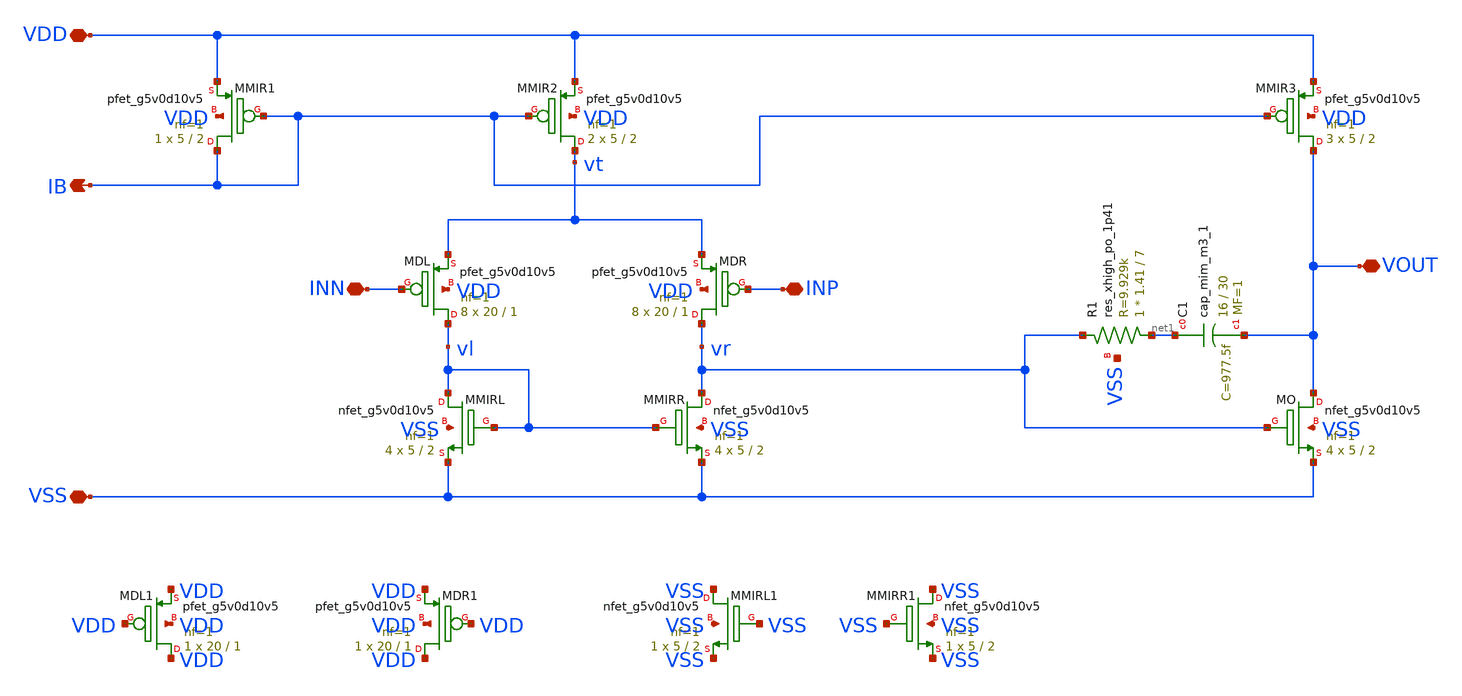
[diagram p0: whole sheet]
** sch_path: tt08/ip/bmbg/xschem/bmbgota.sch
**.subckt bmbgota INP INN VOUT IB VDD VSS
*.iopin INP
*.iopin INN
*.iopin VOUT
*.opin IB
*.iopin VDD
*.iopin VSS
XMDR vr INP vt VDD sky130_fd_pr__pfet_g5v0d10v5 L=1 W=20 nf=1 ad='int((nf+1)/2) * W/nf * 0.29' as='int((nf+2)/2) * W/nf * 0.29'
+ pd='2*int((nf+1)/2) * (W/nf + 0.29)' ps='2*int((nf+2)/2) * (W/nf + 0.29)' nrd='0.29 / W' nrs='0.29 / W'
+ sa=0 sb=0 sd=0 mult=8 m=8
XMMIRL vl vl VSS VSS sky130_fd_pr__nfet_g5v0d10v5 L=2 W=5 nf=1 ad='int((nf+1)/2) * W/nf * 0.29' as='int((nf+2)/2) * W/nf * 0.29'
+ pd='2*int((nf+1)/2) * (W/nf + 0.29)' ps='2*int((nf+2)/2) * (W/nf + 0.29)' nrd='0.29 / W' nrs='0.29 / W'
+ sa=0 sb=0 sd=0 mult=4 m=4
XMMIRR vr vl VSS VSS sky130_fd_pr__nfet_g5v0d10v5 L=2 W=5 nf=1 ad='int((nf+1)/2) * W/nf * 0.29' as='int((nf+2)/2) * W/nf * 0.29'
+ pd='2*int((nf+1)/2) * (W/nf + 0.29)' ps='2*int((nf+2)/2) * (W/nf + 0.29)' nrd='0.29 / W' nrs='0.29 / W'
+ sa=0 sb=0 sd=0 mult=4 m=4
XMDL vl INN vt VDD sky130_fd_pr__pfet_g5v0d10v5 L=1 W=20 nf=1 ad='int((nf+1)/2) * W/nf * 0.29' as='int((nf+2)/2) * W/nf * 0.29'
+ pd='2*int((nf+1)/2) * (W/nf + 0.29)' ps='2*int((nf+2)/2) * (W/nf + 0.29)' nrd='0.29 / W' nrs='0.29 / W'
+ sa=0 sb=0 sd=0 mult=8 m=8
XMMIR2 vt IB VDD VDD sky130_fd_pr__pfet_g5v0d10v5 L=2 W=5 nf=1 ad='int((nf+1)/2) * W/nf * 0.29' as='int((nf+2)/2) * W/nf * 0.29'
+ pd='2*int((nf+1)/2) * (W/nf + 0.29)' ps='2*int((nf+2)/2) * (W/nf + 0.29)' nrd='0.29 / W' nrs='0.29 / W'
+ sa=0 sb=0 sd=0 mult=2 m=2
XMMIR1 IB IB VDD VDD sky130_fd_pr__pfet_g5v0d10v5 L=2 W=5 nf=1 ad='int((nf+1)/2) * W/nf * 0.29' as='int((nf+2)/2) * W/nf * 0.29'
+ pd='2*int((nf+1)/2) * (W/nf + 0.29)' ps='2*int((nf+2)/2) * (W/nf + 0.29)' nrd='0.29 / W' nrs='0.29 / W'
+ sa=0 sb=0 sd=0 mult=1 m=1
XMO VOUT vr VSS VSS sky130_fd_pr__nfet_g5v0d10v5 L=2 W=5 nf=1 ad='int((nf+1)/2) * W/nf * 0.29' as='int((nf+2)/2) * W/nf * 0.29'
+ pd='2*int((nf+1)/2) * (W/nf + 0.29)' ps='2*int((nf+2)/2) * (W/nf + 0.29)' nrd='0.29 / W' nrs='0.29 / W'
+ sa=0 sb=0 sd=0 mult=4 m=4
XMMIR3 VOUT IB VDD VDD sky130_fd_pr__pfet_g5v0d10v5 L=2 W=5 nf=1 ad='int((nf+1)/2) * W/nf * 0.29' as='int((nf+2)/2) * W/nf * 0.29'
+ pd='2*int((nf+1)/2) * (W/nf + 0.29)' ps='2*int((nf+2)/2) * (W/nf + 0.29)' nrd='0.29 / W' nrs='0.29 / W'
+ sa=0 sb=0 sd=0 mult=3 m=3
XR1 net1 vr VSS sky130_fd_pr__res_xhigh_po_1p41 L=7 mult=1 m=1
XC1 net1 VOUT sky130_fd_pr__cap_mim_m3_1 W=16 L=30 MF=1 m=1
XMDL1 VDD VDD VDD VDD sky130_fd_pr__pfet_g5v0d10v5 L=1 W=20 nf=1 ad='int((nf+1)/2) * W/nf * 0.29' as='int((nf+2)/2) * W/nf * 0.29'
+ pd='2*int((nf+1)/2) * (W/nf + 0.29)' ps='2*int((nf+2)/2) * (W/nf + 0.29)' nrd='0.29 / W' nrs='0.29 / W'
+ sa=0 sb=0 sd=0 mult=1 m=1
XMDR1 VDD VDD VDD VDD sky130_fd_pr__pfet_g5v0d10v5 L=1 W=20 nf=1 ad='int((nf+1)/2) * W/nf * 0.29' as='int((nf+2)/2) * W/nf * 0.29'
+ pd='2*int((nf+1)/2) * (W/nf + 0.29)' ps='2*int((nf+2)/2) * (W/nf + 0.29)' nrd='0.29 / W' nrs='0.29 / W'
+ sa=0 sb=0 sd=0 mult=1 m=1
XMMIRL1 VSS VSS VSS VSS sky130_fd_pr__nfet_g5v0d10v5 L=2 W=5 nf=1 ad='int((nf+1)/2) * W/nf * 0.29' as='int((nf+2)/2) * W/nf * 0.29'
+ pd='2*int((nf+1)/2) * (W/nf + 0.29)' ps='2*int((nf+2)/2) * (W/nf + 0.29)' nrd='0.29 / W' nrs='0.29 / W'
+ sa=0 sb=0 sd=0 mult=1 m=1
XMMIRR1 VSS VSS VSS VSS sky130_fd_pr__nfet_g5v0d10v5 L=2 W=5 nf=1 ad='int((nf+1)/2) * W/nf * 0.29' as='int((nf+2)/2) * W/nf * 0.29'
+ pd='2*int((nf+1)/2) * (W/nf + 0.29)' ps='2*int((nf+2)/2) * (W/nf + 0.29)' nrd='0.29 / W' nrs='0.29 / W'
+ sa=0 sb=0 sd=0 mult=1 m=1
**.ends
.end
